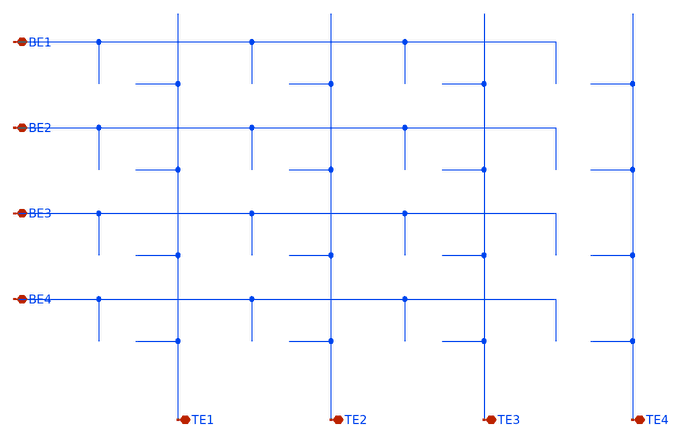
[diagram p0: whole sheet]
** sch_path: libraries/openmemristorpdk_pr/crossbar4x4_tio2_au.sch
**.subckt crossbar4x4_tio2_au BE1 BE2 BE3 BE4 TE1 TE2 TE3 TE4
*.iopin BE1
*.iopin BE2
*.iopin BE3
*.iopin BE4
*.iopin TE1
*.iopin TE2
*.iopin TE3
*.iopin TE4
**.ends
.end
